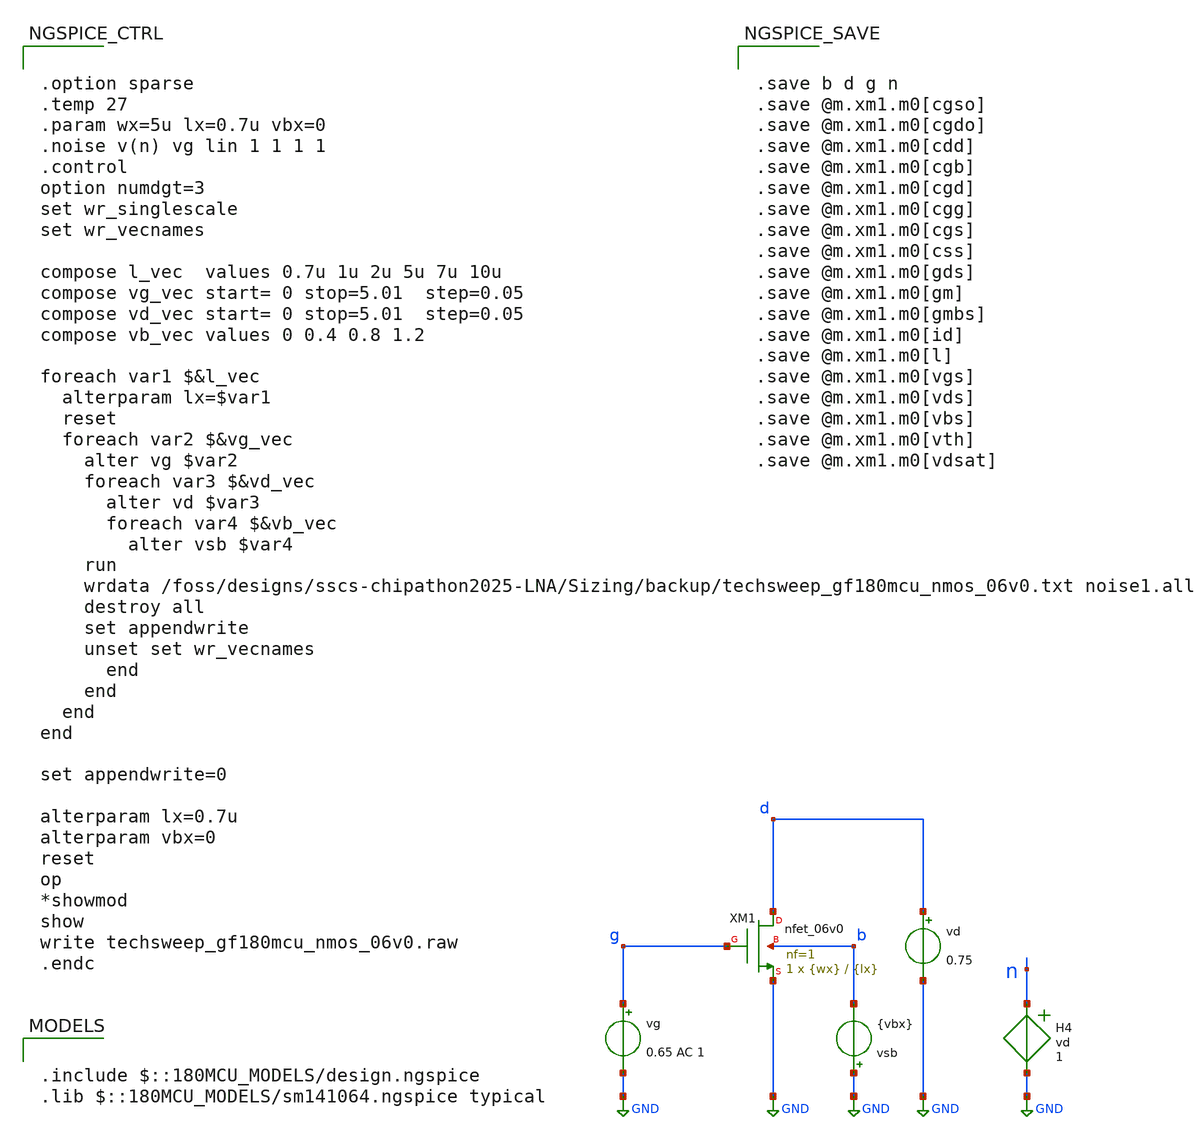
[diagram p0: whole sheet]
** sch_path: Sizing/backup/techsweep_gf180mcu_nmos_5v.sch
* (c) 2025 H. Pretl, Apache-2.0 license
**.subckt techsweep_gf180mcu_nmos_5v
vg g GND 0.65 AC 1
vd d GND 0.75
vsb GND b {vbx}
H4 n GND vd 1
XM1 d g GND b nfet_06v0 L={lx} W={wx} nf=1 ad='int((nf+1)/2) * W/nf * 0.18u' as='int((nf+2)/2) * W/nf * 0.18u'
+ pd='2*int((nf+1)/2) * (W/nf + 0.18u)' ps='2*int((nf+2)/2) * (W/nf + 0.18u)' nrd='0.18u / W' nrs='0.18u / W'
+ sa=0 sb=0 sd=0 m=1
**** begin user architecture code


.option sparse
.temp 27
.param wx=5u lx=0.7u vbx=0
.noise v(n) vg lin 1 1 1 1
.control
option numdgt=3
set wr_singlescale
set wr_vecnames

compose l_vec  values 0.7u 1u 2u 5u 7u 10u
compose vg_vec start= 0 stop=5.01  step=0.05
compose vd_vec start= 0 stop=5.01  step=0.05
compose vb_vec values 0 0.4 0.8 1.2

foreach var1 $&l_vec
  alterparam lx=$var1
  reset
  foreach var2 $&vg_vec
    alter vg $var2
    foreach var3 $&vd_vec
      alter vd $var3
      foreach var4 $&vb_vec
        alter vsb $var4
	run
	wrdata /foss/designs/sscs-chipathon2025-LNA/Sizing/backup/techsweep_gf180mcu_nmos_06v0.txt
+ noise1.all
	destroy all
	set appendwrite
	unset set wr_vecnames
      end
    end
  end
end

set appendwrite=0

alterparam lx=0.7u
alterparam vbx=0
reset
op
*showmod
show
write techsweep_gf180mcu_nmos_06v0.raw
.endc




.save b d g n
.save @m.xm1.m0[cgso]
.save @m.xm1.m0[cgdo]
.save @m.xm1.m0[cdd]
.save @m.xm1.m0[cgb]
.save @m.xm1.m0[cgd]
.save @m.xm1.m0[cgg]
.save @m.xm1.m0[cgs]
.save @m.xm1.m0[css]
.save @m.xm1.m0[gds]
.save @m.xm1.m0[gm]
.save @m.xm1.m0[gmbs]
.save @m.xm1.m0[id]
.save @m.xm1.m0[l]
.save @m.xm1.m0[vgs]
.save @m.xm1.m0[vds]
.save @m.xm1.m0[vbs]
.save @m.xm1.m0[vth]
.save @m.xm1.m0[vdsat]



.include $::180MCU_MODELS/design.ngspice
.lib $::180MCU_MODELS/sm141064.ngspice typical

**** end user architecture code
**.ends
.GLOBAL GND
.end
